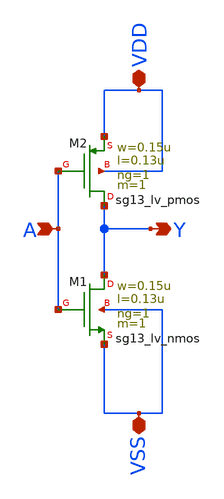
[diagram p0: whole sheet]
** sch_path: BTDay6-Ex/inverter.sch
**.subckt inverter A Y VDD VSS
*.ipin A
*.opin Y
*.iopin VDD
*.iopin VSS
XM1 Y A VSS VSS sg13_lv_nmos w=0.15u l=0.13u ng=1 m=1 mm_ok=1
XM2 Y A VDD VDD sg13_lv_pmos w=0.15u l=0.13u ng=1 m=1 mm_ok=1
**.ends
.end
